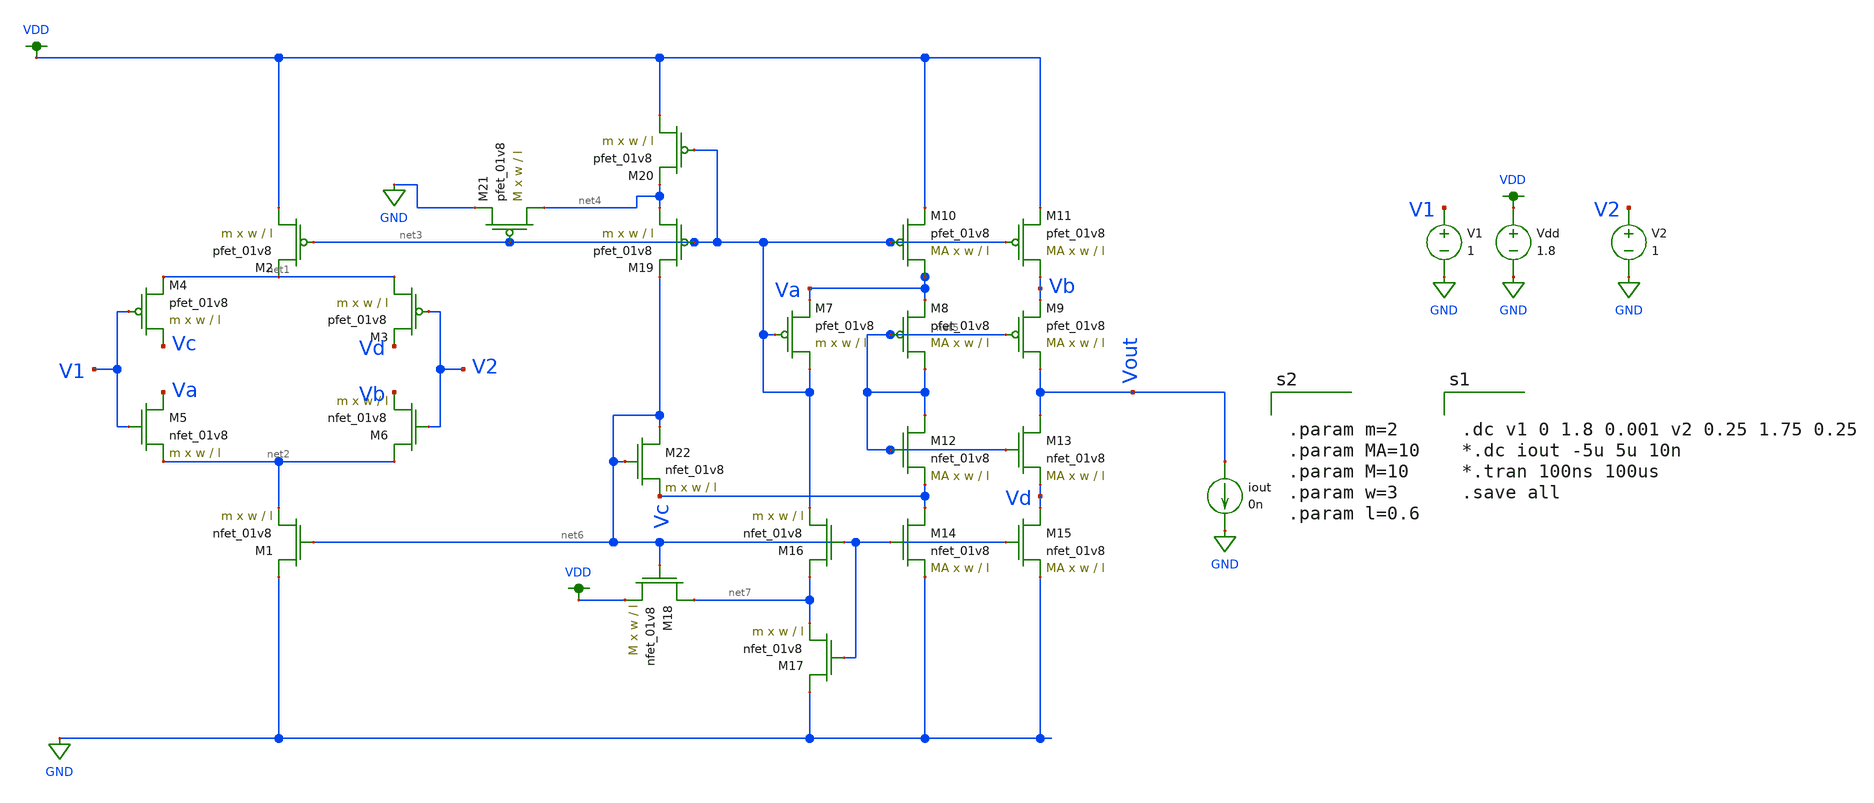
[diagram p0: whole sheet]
** sch_path: schematics/opamp_new.sch
**.subckt opamp_new
Vdd VDD GND 1.8
V1 V1 GND 1
iout Vout GND 0n
XM1 GND net6 net2 GND sky130_fd_pr__nfet_01v8 L=l W=w nf=1 ad='int((nf+1)/2) * W/nf * 0.29' as='int((nf+2)/2) * W/nf * 0.29'
+ pd='2*int((nf+1)/2) * (W/nf + 0.29)' ps='2*int((nf+2)/2) * (W/nf + 0.29)' nrd='0.29 / W' nrs='0.29 / W'
+ sa=0 sb=0 sd=0 mult=m m=m
XM2 VDD net3 net1 VDD sky130_fd_pr__pfet_01v8 L=l W=w nf=1 ad='int((nf+1)/2) * W/nf * 0.29' as='int((nf+2)/2) * W/nf * 0.29'
+ pd='2*int((nf+1)/2) * (W/nf + 0.29)' ps='2*int((nf+2)/2) * (W/nf + 0.29)' nrd='0.29 / W' nrs='0.29 / W'
+ sa=0 sb=0 sd=0 mult=m m=m
XM3 net1 V2 Vd VDD sky130_fd_pr__pfet_01v8 L=l W=w nf=1 ad='int((nf+1)/2) * W/nf * 0.29' as='int((nf+2)/2) * W/nf * 0.29'
+ pd='2*int((nf+1)/2) * (W/nf + 0.29)' ps='2*int((nf+2)/2) * (W/nf + 0.29)' nrd='0.29 / W' nrs='0.29 / W'
+ sa=0 sb=0 sd=0 mult=m m=m
XM4 Vc V1 net1 VDD sky130_fd_pr__pfet_01v8 L=l W=w nf=1 ad='int((nf+1)/2) * W/nf * 0.29' as='int((nf+2)/2) * W/nf * 0.29'
+ pd='2*int((nf+1)/2) * (W/nf + 0.29)' ps='2*int((nf+2)/2) * (W/nf + 0.29)' nrd='0.29 / W' nrs='0.29 / W'
+ sa=0 sb=0 sd=0 mult=m m=m
XM5 Va V1 net2 GND sky130_fd_pr__nfet_01v8 L=l W=w nf=1 ad='int((nf+1)/2) * W/nf * 0.29' as='int((nf+2)/2) * W/nf * 0.29'
+ pd='2*int((nf+1)/2) * (W/nf + 0.29)' ps='2*int((nf+2)/2) * (W/nf + 0.29)' nrd='0.29 / W' nrs='0.29 / W'
+ sa=0 sb=0 sd=0 mult=m m=m
XM6 net2 V2 Vb GND sky130_fd_pr__nfet_01v8 L=l W=w nf=1 ad='int((nf+1)/2) * W/nf * 0.29' as='int((nf+2)/2) * W/nf * 0.29'
+ pd='2*int((nf+1)/2) * (W/nf + 0.29)' ps='2*int((nf+2)/2) * (W/nf + 0.29)' nrd='0.29 / W' nrs='0.29 / W'
+ sa=0 sb=0 sd=0 mult=m m=m
XM7 net3 net3 Va VDD sky130_fd_pr__pfet_01v8 L=l W=w nf=1 ad='int((nf+1)/2) * W/nf * 0.29' as='int((nf+2)/2) * W/nf * 0.29'
+ pd='2*int((nf+1)/2) * (W/nf + 0.29)' ps='2*int((nf+2)/2) * (W/nf + 0.29)' nrd='0.29 / W' nrs='0.29 / W'
+ sa=0 sb=0 sd=0 mult=m m=m
XM8 net5 net5 Va VDD sky130_fd_pr__pfet_01v8 L=l W=w nf=1 ad='int((nf+1)/2) * W/nf * 0.29' as='int((nf+2)/2) * W/nf * 0.29'
+ pd='2*int((nf+1)/2) * (W/nf + 0.29)' ps='2*int((nf+2)/2) * (W/nf + 0.29)' nrd='0.29 / W' nrs='0.29 / W'
+ sa=0 sb=0 sd=0 mult=MA m=MA
XM9 Vout net5 Vb VDD sky130_fd_pr__pfet_01v8 L=l W=w nf=1 ad='int((nf+1)/2) * W/nf * 0.29' as='int((nf+2)/2) * W/nf * 0.29'
+ pd='2*int((nf+1)/2) * (W/nf + 0.29)' ps='2*int((nf+2)/2) * (W/nf + 0.29)' nrd='0.29 / W' nrs='0.29 / W'
+ sa=0 sb=0 sd=0 mult=MA m=MA
XM10 Va net3 VDD VDD sky130_fd_pr__pfet_01v8 L=l W=w nf=1 ad='int((nf+1)/2) * W/nf * 0.29' as='int((nf+2)/2) * W/nf * 0.29'
+ pd='2*int((nf+1)/2) * (W/nf + 0.29)' ps='2*int((nf+2)/2) * (W/nf + 0.29)' nrd='0.29 / W' nrs='0.29 / W'
+ sa=0 sb=0 sd=0 mult=MA m=MA
XM11 Vb net3 VDD VDD sky130_fd_pr__pfet_01v8 L=l W=w nf=1 ad='int((nf+1)/2) * W/nf * 0.29' as='int((nf+2)/2) * W/nf * 0.29'
+ pd='2*int((nf+1)/2) * (W/nf + 0.29)' ps='2*int((nf+2)/2) * (W/nf + 0.29)' nrd='0.29 / W' nrs='0.29 / W'
+ sa=0 sb=0 sd=0 mult=MA m=MA
XM12 net5 net5 Vc GND sky130_fd_pr__nfet_01v8 L=l W=w nf=1 ad='int((nf+1)/2) * W/nf * 0.29' as='int((nf+2)/2) * W/nf * 0.29'
+ pd='2*int((nf+1)/2) * (W/nf + 0.29)' ps='2*int((nf+2)/2) * (W/nf + 0.29)' nrd='0.29 / W' nrs='0.29 / W'
+ sa=0 sb=0 sd=0 mult=MA m=MA
XM13 Vout net5 Vd GND sky130_fd_pr__nfet_01v8 L=l W=w nf=1 ad='int((nf+1)/2) * W/nf * 0.29' as='int((nf+2)/2) * W/nf * 0.29'
+ pd='2*int((nf+1)/2) * (W/nf + 0.29)' ps='2*int((nf+2)/2) * (W/nf + 0.29)' nrd='0.29 / W' nrs='0.29 / W'
+ sa=0 sb=0 sd=0 mult=MA m=MA
XM14 Vc net6 GND GND sky130_fd_pr__nfet_01v8 L=l W=w nf=1 ad='int((nf+1)/2) * W/nf * 0.29' as='int((nf+2)/2) * W/nf * 0.29'
+ pd='2*int((nf+1)/2) * (W/nf + 0.29)' ps='2*int((nf+2)/2) * (W/nf + 0.29)' nrd='0.29 / W' nrs='0.29 / W'
+ sa=0 sb=0 sd=0 mult=MA m=MA
XM15 Vd net6 GND GND sky130_fd_pr__nfet_01v8 L=l W=w nf=1 ad='int((nf+1)/2) * W/nf * 0.29' as='int((nf+2)/2) * W/nf * 0.29'
+ pd='2*int((nf+1)/2) * (W/nf + 0.29)' ps='2*int((nf+2)/2) * (W/nf + 0.29)' nrd='0.29 / W' nrs='0.29 / W'
+ sa=0 sb=0 sd=0 mult=MA m=MA
XM16 net7 net6 net3 GND sky130_fd_pr__nfet_01v8 L=l W=w nf=1 ad='int((nf+1)/2) * W/nf * 0.29' as='int((nf+2)/2) * W/nf * 0.29'
+ pd='2*int((nf+1)/2) * (W/nf + 0.29)' ps='2*int((nf+2)/2) * (W/nf + 0.29)' nrd='0.29 / W' nrs='0.29 / W'
+ sa=0 sb=0 sd=0 mult=m m=m
XM17 GND net6 net7 GND sky130_fd_pr__nfet_01v8 L=l W=w nf=1 ad='int((nf+1)/2) * W/nf * 0.29' as='int((nf+2)/2) * W/nf * 0.29'
+ pd='2*int((nf+1)/2) * (W/nf + 0.29)' ps='2*int((nf+2)/2) * (W/nf + 0.29)' nrd='0.29 / W' nrs='0.29 / W'
+ sa=0 sb=0 sd=0 mult=m m=m
XM18 net7 net6 VDD GND sky130_fd_pr__nfet_01v8 L=l W=w nf=1 ad='int((nf+1)/2) * W/nf * 0.29' as='int((nf+2)/2) * W/nf * 0.29'
+ pd='2*int((nf+1)/2) * (W/nf + 0.29)' ps='2*int((nf+2)/2) * (W/nf + 0.29)' nrd='0.29 / W' nrs='0.29 / W'
+ sa=0 sb=0 sd=0 mult=M m=M
XM19 net4 net3 net6 VDD sky130_fd_pr__pfet_01v8 L=l W=w nf=1 ad='int((nf+1)/2) * W/nf * 0.29' as='int((nf+2)/2) * W/nf * 0.29'
+ pd='2*int((nf+1)/2) * (W/nf + 0.29)' ps='2*int((nf+2)/2) * (W/nf + 0.29)' nrd='0.29 / W' nrs='0.29 / W'
+ sa=0 sb=0 sd=0 mult=m m=m
XM20 VDD net3 net4 VDD sky130_fd_pr__pfet_01v8 L=l W=w nf=1 ad='int((nf+1)/2) * W/nf * 0.29' as='int((nf+2)/2) * W/nf * 0.29'
+ pd='2*int((nf+1)/2) * (W/nf + 0.29)' ps='2*int((nf+2)/2) * (W/nf + 0.29)' nrd='0.29 / W' nrs='0.29 / W'
+ sa=0 sb=0 sd=0 mult=m m=m
XM21 net4 net3 GND VDD sky130_fd_pr__pfet_01v8 L=l W=w nf=1 ad='int((nf+1)/2) * W/nf * 0.29' as='int((nf+2)/2) * W/nf * 0.29'
+ pd='2*int((nf+1)/2) * (W/nf + 0.29)' ps='2*int((nf+2)/2) * (W/nf + 0.29)' nrd='0.29 / W' nrs='0.29 / W'
+ sa=0 sb=0 sd=0 mult=M m=M
XM22 net6 net6 Vc GND sky130_fd_pr__nfet_01v8 L=l W=w nf=1 ad='int((nf+1)/2) * W/nf * 0.29' as='int((nf+2)/2) * W/nf * 0.29'
+ pd='2*int((nf+1)/2) * (W/nf + 0.29)' ps='2*int((nf+2)/2) * (W/nf + 0.29)' nrd='0.29 / W' nrs='0.29 / W'
+ sa=0 sb=0 sd=0 mult=m m=m
V2 V2 GND 1
**** begin user architecture code

.option wnflag=1
.param MC_SWITCH=0.0
.lib ~/skywater/skywater-pdk/libraries/sky130_fd_pr_ngspice/latest/models/sky130.lib.spice tt



.dc v1 0 1.8 0.001 v2 0.25 1.75 0.25
*.dc iout -5u 5u 10n
*.tran 100ns 100us
.save all




.param m=2
.param MA=10
.param M=10
.param w=3
.param l=0.6


**** end user architecture code
**.ends
.GLOBAL GND
.GLOBAL VDD
.end
